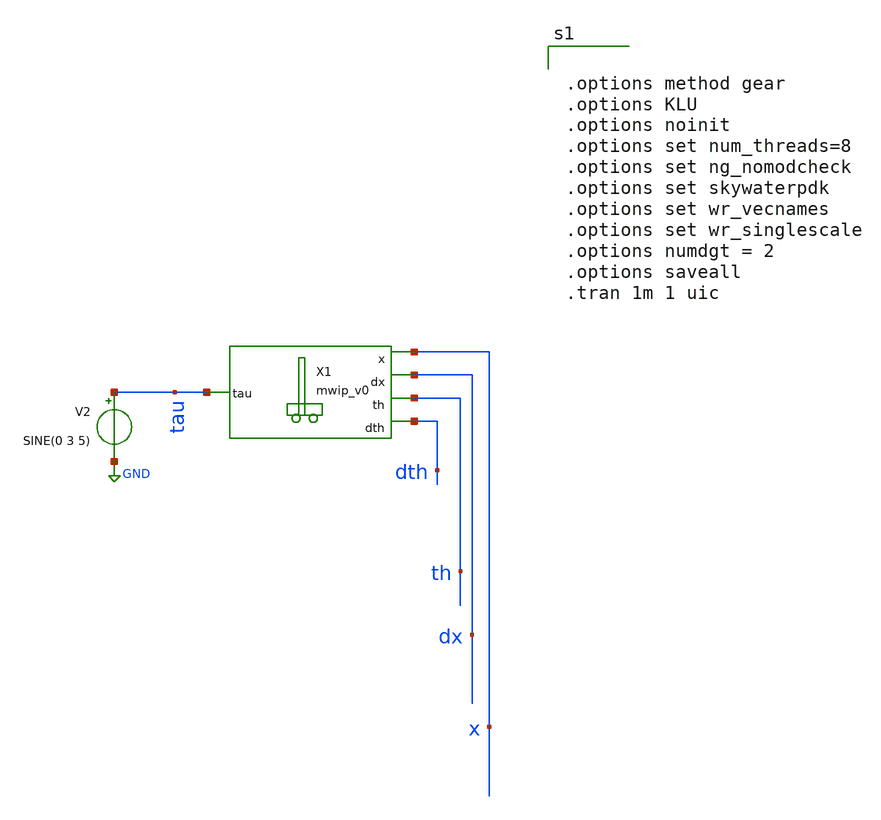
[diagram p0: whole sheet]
** sch_path: tb_mwip.sch
**.subckt tb_mwip
V2 tau GND SINE(0 3 5)
XX1 tau x th dx dth mwip_v0
**** begin user architecture code

*MADE BY JORGE ALEJANDRO JUAREZ LORA IPN


.subckt mwip_v0 tau x th dx dth
    N1 Tau x th dx dth mwip_v0_model
.ends mwip_v0

.model mwip_v0_model mwip_dynamics

.control

    pre_osdi /foss/designs/SNN-MWIP/MWIP/mwip.osdi
.endc



.options method gear
.options KLU
.options noinit
.options set num_threads=8
.options set ng_nomodcheck
.options set skywaterpdk
.options set wr_vecnames
.options set wr_singlescale
.options numdgt = 2
.options saveall
.tran 1m 1 uic



**** end user architecture code
**.ends
.GLOBAL GND
.end
